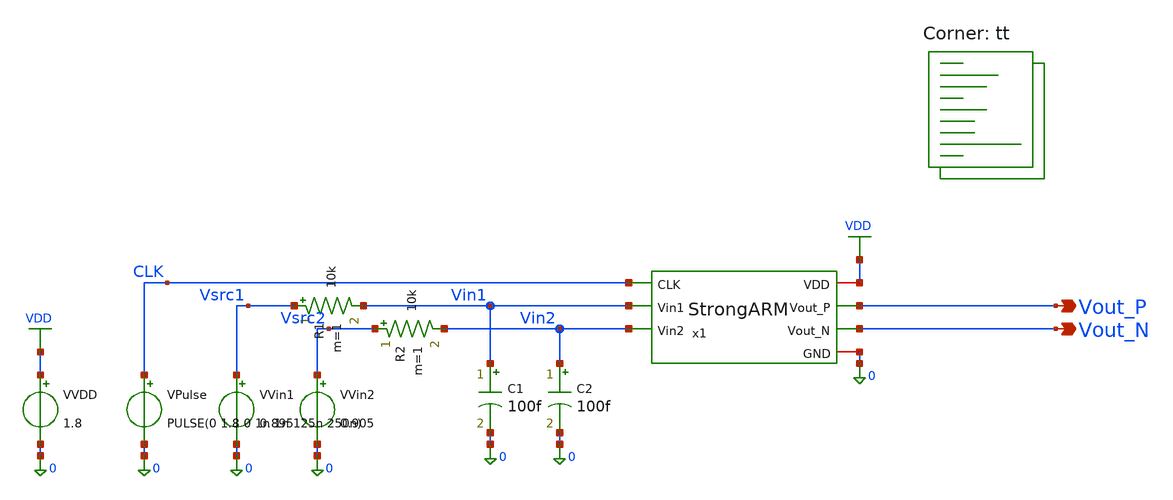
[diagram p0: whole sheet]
** sch_path: blocks/03_StrongARM/sim/tb_StrongARM_Kickback.sch
**.subckt tb_StrongARM_Kickback Vout_P Vout_N
*.opin Vout_P
*.opin Vout_N
x1 VDD CLK Vout_P Vout_N Vin1 Vin2 0 StrongARM
VVDD VDD 0 1.8
VVin1 Vsrc1 0 0.895
VVin2 Vsrc2 0 0.905
VPulse CLK 0 PULSE(0 1.8 0 1n 1n 125n 250n)
R1 Vsrc1 Vin1 10k m=1
R2 Vsrc2 Vin2 10k m=1
C1 Vin1 0 100f m=1
C2 Vin2 0 100f m=1
**** begin user architecture code
.lib $::SKYWATER_MODELS/sky130.lib.spice tt



.control
save all

* ============================================
* BLOCK 3 - STRONGARM COMPARATOR
* TEST 7B - AUTOMATED KICKBACK SWEEP
* SKY130 TT / VDD 1.8V / CLK 4MHz
* 9 RC COMBINATIONS / 2 POLARITIES
* ============================================

echo ============================================
echo STRONGARM AUTOMATED KICKBACK TEST 7B
echo ============================================

foreach r 1k 10k 100k

  foreach c 50f 100f 500f

    * Apply identical source impedance
    alter R1 $r
    alter R2 $r
    alter C1 $c
    alter C2 $c

    foreach dv -0.01 0.01

      setplot const

      let vip = 0.9 + ($dv / 2)
      let vin = 0.9 - ($dv / 2)

      alter VVin1 $&vip
      alter VVin2 $&vin

      echo
      echo ============================================
      echo RC CONFIGURATION
      echo Rsource = $r
      echo Csource = $c
      echo Differential input = $dv
      echo ============================================

      * Run transient through reset and evaluation
      tran 0.05n 2.25u

      * Input disturbances relative to ideal sources
      let d1 = v(vin1) - v(vsrc1)
      let d2 = v(vin2) - v(vsrc2)

      * Differential and common-mode kickback
      let kbdiff = d1 - d2
      let kbcm = (d1 + d2) / 2

      let absdiff = abs(kbdiff)
      let abscm = abs(kbcm)

      * Before clock evaluation
      meas tran vin1_pre FIND v(vin1) AT=1.99u
      meas tran vin2_pre FIND v(vin2) AT=1.99u

      * Evaluation rising edge at 2us
      meas tran kb_eval MAX absdiff FROM=2u TO=2.02u
      meas tran kb_common MAX abscm FROM=2u TO=2.02u

      * Reset falling edge at 2.125us
      meas tran kb_reset MAX absdiff FROM=2.125u TO=2.145u

      * Check comparator decision
      meas tran vp_eval FIND v(vout_p) AT=2.01u
      meas tran vn_eval FIND v(vout_n) AT=2.01u

      * Check settled decision
      meas tran vp_late FIND v(vout_p) AT=2.08u
      meas tran vn_late FIND v(vout_n) AT=2.08u

      * Check reset
      meas tran vp_reset FIND v(vout_p) AT=2.20u
      meas tran vn_reset FIND v(vout_n) AT=2.20u

      * Convert results to millivolts
      let kb_eval_mV = kb_eval * 1e3
      let kb_reset_mV = kb_reset * 1e3
      let kb_common_mV = kb_common * 1e3

      echo ============================================
      echo KICKBACK RESULTS IN mV
      echo ============================================

      print kb_eval_mV
      print kb_reset_mV
      print kb_common_mV

      echo ============================================
      echo OUTPUT DECISION RESULTS
      echo ============================================

      print vp_eval
      print vn_eval
      print vp_late
      print vn_late

      echo ============================================
      echo END OF CONFIGURATION
      echo ============================================

    end

  end

end

echo
echo ============================================
echo ALL 18 KICKBACK SIMULATIONS COMPLETED
echo ============================================
echo

.endc

**** end user architecture code
**.ends

* expanding   symbol:  blocks/03_StrongARM/xschem/StrongARM.sym # of pins=7
** sym_path: blocks/03_StrongARM/xschem/StrongARM.sym
** sch_path: blocks/03_StrongARM/xschem/StrongARM.sch
.subckt StrongARM VDD CLK Vout_P Vout_N Vin1 Vin2 GND
*.iopin VDD
*.iopin GND
*.ipin Vin1
*.ipin Vin2
*.ipin CLK
*.opin Vout_P
*.opin Vout_N
XS1 P CLK VDD VDD sky130_fd_pr__pfet_01v8 L=0.15 W=1.5 nf=1 ad='int((1 + 1)/2) * 1.5 / 1 * 0.29' as='int((1 + 2)/2) * 1.5 / 1 * 0.29'
+ pd='2*int((1 + 1)/2) * (1.5 / 1 + 0.29)' ps='2*int((1 + 2)/2) * (1.5 / 1 + 0.29)' nrd='0.29 / 1.5 ' nrs='0.29 / 1.5 '
+ sa=0 sb=0 sd=0 mult=1 m=1
XS3 Vout_P CLK VDD VDD sky130_fd_pr__pfet_01v8 L=0.15 W=1.5 nf=1 ad='int((1 + 1)/2) * 1.5 / 1 * 0.29'
+ as='int((1 + 2)/2) * 1.5 / 1 * 0.29' pd='2*int((1 + 1)/2) * (1.5 / 1 + 0.29)' ps='2*int((1 + 2)/2) * (1.5 / 1 + 0.29)'
+ nrd='0.29 / 1.5 ' nrs='0.29 / 1.5 ' sa=0 sb=0 sd=0 mult=1 m=1
XM5 Vout_P Vout_N VDD VDD sky130_fd_pr__pfet_01v8 L=0.3 W=5 nf=1 ad='int((1 + 1)/2) * 5 / 1 * 0.29' as='int((1 + 2)/2) * 5 / 1 * 0.29'
+ pd='2*int((1 + 1)/2) * (5 / 1 + 0.29)' ps='2*int((1 + 2)/2) * (5 / 1 + 0.29)' nrd='0.29 / 5 ' nrs='0.29 / 5 '
+ sa=0 sb=0 sd=0 mult=1 m=1
XM6 Vout_N Vout_P VDD VDD sky130_fd_pr__pfet_01v8 L=0.3 W=5 nf=1 ad='int((1 + 1)/2) * 5 / 1 * 0.29' as='int((1 + 2)/2) * 5 / 1 * 0.29'
+ pd='2*int((1 + 1)/2) * (5 / 1 + 0.29)' ps='2*int((1 + 2)/2) * (5 / 1 + 0.29)' nrd='0.29 / 5 ' nrs='0.29 / 5 '
+ sa=0 sb=0 sd=0 mult=1 m=1
XS4 Vout_N CLK VDD VDD sky130_fd_pr__pfet_01v8 L=0.15 W=1.5 nf=1 ad='int((1 + 1)/2) * 1.5 / 1 * 0.29'
+ as='int((1 + 2)/2) * 1.5 / 1 * 0.29' pd='2*int((1 + 1)/2) * (1.5 / 1 + 0.29)' ps='2*int((1 + 2)/2) * (1.5 / 1 + 0.29)'
+ nrd='0.29 / 1.5 ' nrs='0.29 / 1.5 ' sa=0 sb=0 sd=0 mult=1 m=1
XS2 Q CLK VDD VDD sky130_fd_pr__pfet_01v8 L=0.15 W=1.5 nf=1 ad='int((1 + 1)/2) * 1.5 / 1 * 0.29' as='int((1 + 2)/2) * 1.5 / 1 * 0.29'
+ pd='2*int((1 + 1)/2) * (1.5 / 1 + 0.29)' ps='2*int((1 + 2)/2) * (1.5 / 1 + 0.29)' nrd='0.29 / 1.5 ' nrs='0.29 / 1.5 '
+ sa=0 sb=0 sd=0 mult=1 m=1
XM3 Vout_P Vout_N P GND sky130_fd_pr__nfet_01v8 L=0.3 W=2 nf=1 ad='int((1 + 1)/2) * 2 / 1 * 0.29' as='int((1 + 2)/2) * 2 / 1 * 0.29'
+ pd='2*int((1 + 1)/2) * (2 / 1 + 0.29)' ps='2*int((1 + 2)/2) * (2 / 1 + 0.29)' nrd='0.29 / 2 ' nrs='0.29 / 2 '
+ sa=0 sb=0 sd=0 mult=1 m=1
XM4 Vout_N Vout_P Q GND sky130_fd_pr__nfet_01v8 L=0.3 W=2 nf=1 ad='int((1 + 1)/2) * 2 / 1 * 0.29' as='int((1 + 2)/2) * 2 / 1 * 0.29'
+ pd='2*int((1 + 1)/2) * (2 / 1 + 0.29)' ps='2*int((1 + 2)/2) * (2 / 1 + 0.29)' nrd='0.29 / 2 ' nrs='0.29 / 2 '
+ sa=0 sb=0 sd=0 mult=1 m=1
XM1 P Vin1 TAIL GND sky130_fd_pr__nfet_01v8 L=0.5 W=10 nf=1 ad='int((1 + 1)/2) * 10 / 1 * 0.29' as='int((1 + 2)/2) * 10 / 1 * 0.29'
+ pd='2*int((1 + 1)/2) * (10 / 1 + 0.29)' ps='2*int((1 + 2)/2) * (10 / 1 + 0.29)' nrd='0.29 / 10 ' nrs='0.29 / 10 '
+ sa=0 sb=0 sd=0 mult=1 m=1
XM2 Q Vin2 TAIL GND sky130_fd_pr__nfet_01v8 L=0.5 W=10 nf=1 ad='int((1 + 1)/2) * 10 / 1 * 0.29' as='int((1 + 2)/2) * 10 / 1 * 0.29'
+ pd='2*int((1 + 1)/2) * (10 / 1 + 0.29)' ps='2*int((1 + 2)/2) * (10 / 1 + 0.29)' nrd='0.29 / 10 ' nrs='0.29 / 10 '
+ sa=0 sb=0 sd=0 mult=1 m=1
XM7 TAIL CLK GND GND sky130_fd_pr__nfet_01v8 L=0.3 W=1 nf=1 ad='int((1 + 1)/2) * 1 / 1 * 0.29' as='int((1 + 2)/2) * 1 / 1 * 0.29'
+ pd='2*int((1 + 1)/2) * (1 / 1 + 0.29)' ps='2*int((1 + 2)/2) * (1 / 1 + 0.29)' nrd='0.29 / 1 ' nrs='0.29 / 1 '
+ sa=0 sb=0 sd=0 mult=1 m=1
.ends

.GLOBAL VDD
.end
